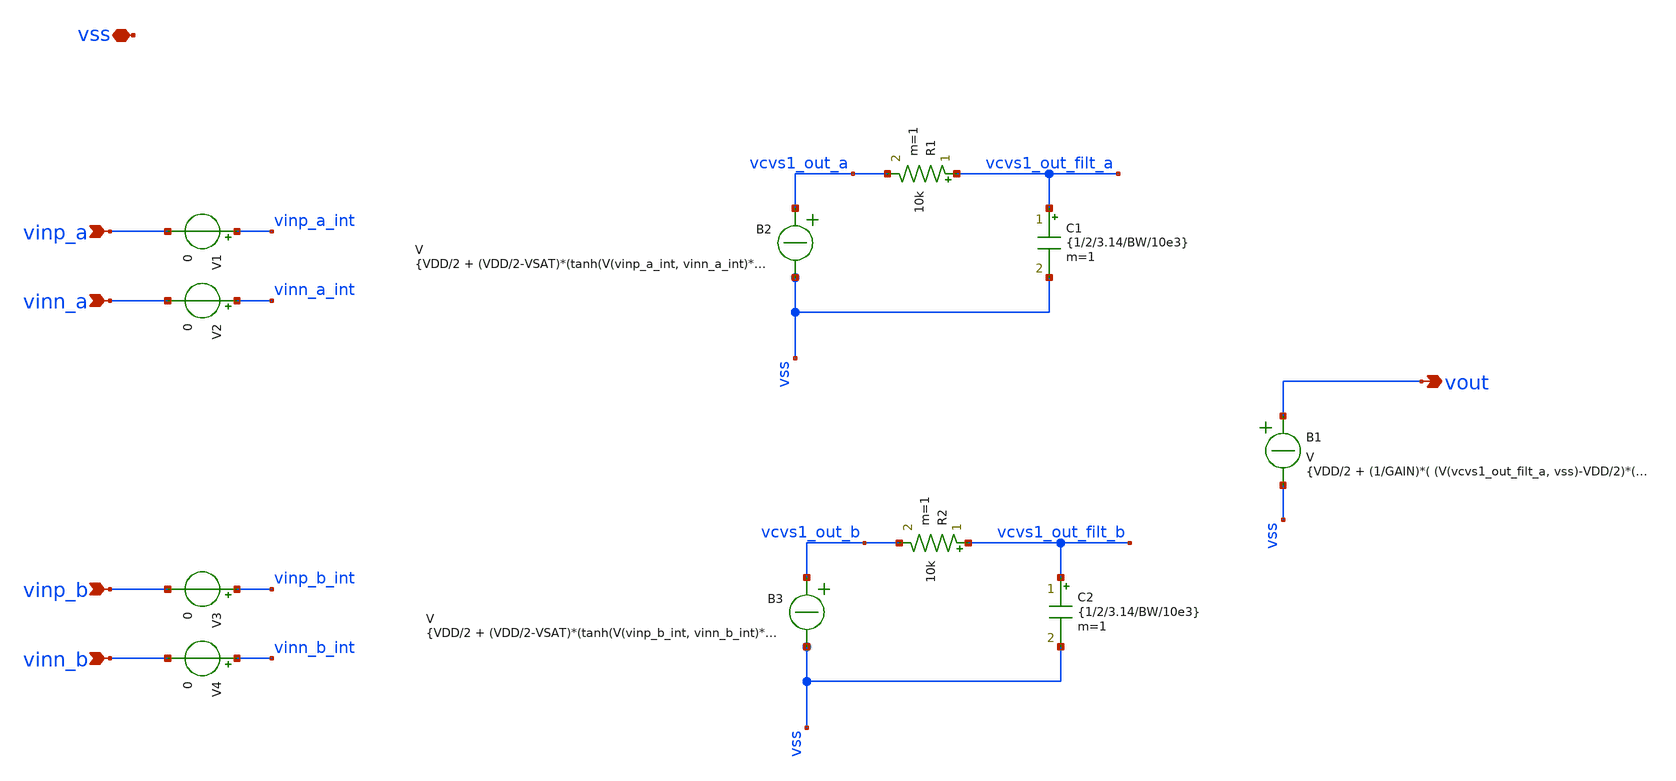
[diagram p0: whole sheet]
** sch_path: xsch/behavioral/multiplier_more_detail.sch
**.subckt multiplier_more_detail vinp_a vinn_a vout vss vinp_b vinn_b
*.ipin vinp_a
*.ipin vinn_a
*.opin vout
*.iopin vss
*.ipin vinp_b
*.ipin vinn_b
R1 vcvs1_out_filt_a vcvs1_out_a 10k m=1
C1 vcvs1_out_filt_a vss {1/2/3.14/BW/10e3} m=1
V1 vinp_a_int vinp_a 0
V2 vinn_a_int vinn_a 0
B2 vcvs1_out_a vss V = {VDD/2 + (VDD/2-VSAT)*(tanh(V(vinp_a_int, vinn_a_int)*1/(VDD/2-VSAT)))}
B1 vout vss V = {VDD/2 + (1/GAIN)*( (V(vcvs1_out_filt_a, vss)-VDD/2)*(V(vcvs1_out_filt_b,vss)-VDD/2) )}
V3 vinp_b_int vinp_b 0
V4 vinn_b_int vinn_b 0
R2 vcvs1_out_filt_b vcvs1_out_b 10k m=1
C2 vcvs1_out_filt_b vss {1/2/3.14/BW/10e3} m=1
B3 vcvs1_out_b vss V = {VDD/2 + (VDD/2-VSAT)*(tanh(V(vinp_b_int, vinn_b_int)*1/(VDD/2-VSAT)))}
**.ends
.end
